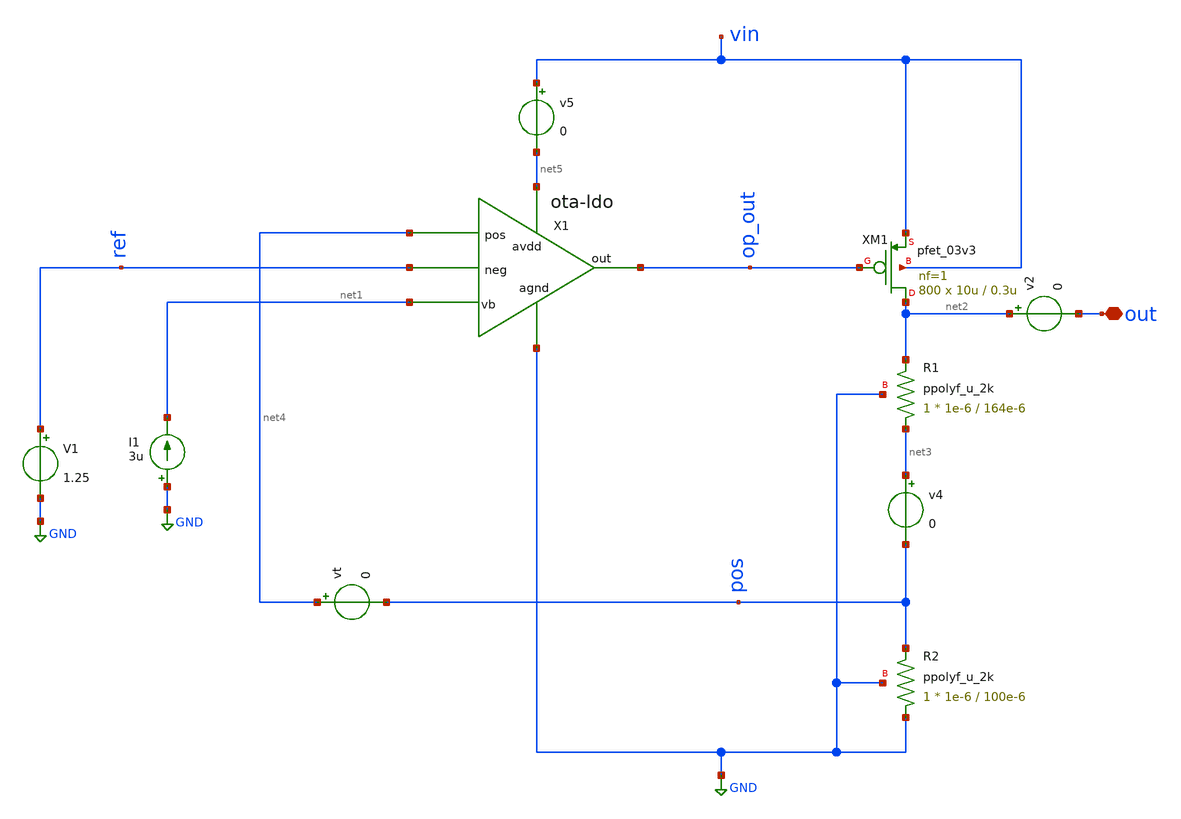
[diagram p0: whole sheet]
** sch_path: LDO/xschem/ldo/test/ldo-full-test.sch

.include $env(PDK_ROOT)/$env(PDK)/libs.tech/ngspice/design.ngspice
.lib $env(PDK_ROOT)/$env(PDK)/libs.tech/ngspice/sm141064.ngspice typical
.lib $env(PDK_ROOT)/$env(PDK)/libs.tech/ngspice/sm141064.ngspice mimcap_statistical
.lib $env(PDK_ROOT)/$env(PDK)/libs.tech/ngspice/sm141064.ngspice cap_mim
.lib $env(PDK_ROOT)/$env(PDK)/libs.tech/ngspice/sm141064.ngspice res_typical

**.subckt ldo-full-test out
*.iopin out
I1 GND net1 3u
V1 ref GND 1.25
XM1 net2 op_out vin vin pfet_03v3 L=0.3u W=10u nf=1 ad='int((nf+1)/2) * W/nf * 0.18u' as='int((nf+2)/2) * W/nf * 0.18u'
+ pd='2*int((nf+1)/2) * (W/nf + 0.18u)' ps='2*int((nf+2)/2) * (W/nf + 0.18u)' nrd='0.18u / W' nrs='0.18u / W'
+ sa=0 sb=0 sd=0 m=800
XR1 net3 net2 GND ppolyf_u_2k r_width=1e-6 r_length=164e-6 m=1
XR2 GND pos GND ppolyf_u_2k r_width=1e-6 r_length=100e-6 m=1
v4 net3 pos 0
X1 net5 op_out ref net4 net1 GND ota-ldo
vt net4 pos 0
v2 net2 out 0
v5 vin net5 0
**** begin user architecture code

.param R=66k
R10 out 0 {R}
IL out 0 PWL(0 0.1m 10u 0.1m 20u 10m 30u 10m)
*CL out 0 10p

Vs vin 0 PULSE(5 5 50u 20u 1u 100u 100u)

.nodeset v(out)=0
.nodeset v(x1.pos)=0

*TRANSIENT
.control
save all
tran 1ns 200us
let gds = @x1.xm2.m0[gds]
print ic
plot gds
plot v(out) v(ref) v(pos) v(vin)
plot i(v5)
*plot v(op_out)
*plot v(out)
*plot i(out)
*plot i(v3)*v(vin)
.endc



*SUPPLY SWEEP
.control
dc Vs 4 0 -0.01
plot v(out) v(ref) v(vin)
*plot v(x1.op_out)
*plot i(v.x1.v4)
.endc

*Stability_Analysis (openloop)
.control
alter Vs AC=0
alter Vt AC =1
ac dec 100 1 1G
plot vdb(out)
let phase_val = 180/PI*cph(out)
plot phase_val
meas ac pm FIND phase_val WHEN vdb(out)=0
*plot (180/pi)*vp(out)
*let gm0=@m.xm0.m0[gm]
*let Zout=(1.5)/(gm0*v(op_out))
*let Zout2=v(out)/gm0
*plot vdb(Zout2)
*wrdata /foss/designs/LDO_Design/data/data_PSRR.dat vdb(out)
.endc

*PSRR_Analysis
.control
alter Vs AC =1
alter Vt AC=0
ac dec 100 1 1G
plot vdb(out)
let phase_val = 180/PI*cph(out)
plot phase_val
*plot (180/pi)*vp(out)
*let gm0=@m.xm0.m0[gm]
*let Zout=(1.5)/(gm0*v(op_out))
*let Zout2=v(out)/gm0
*plot vdb(Zout2)
*wrdata /foss/designs/LDO_Design/data/data_PSRR.dat vdb(out)
.endc


**Load_Transient
.control
alter IL 50u
alter R10 3600k
tran 0.1u 100u
meas TRAN V_ldo_100u FIND v(out) AT=5u
meas TRAN V_ldo_10m FIND v(out) AT=100u
let load_reg= V_ldo_100u-V_ldo_10m
let load_current =(-1*i(Vs)-131.8e-6)
print load_reg
plot i(v2) v(out)-3.3
.endc



.control
alter R10 36k
alter @IL[pwl]=[ 0 0 10u 0 20u 0 30u 0 ]
alter @Vs[pulse]=[4 3.3 50u 1u 1u 10u 100u]
alter IL 0
tran 0.1u 100u
plot v(vin) v(out)
.endc

**** end user architecture code
**.ends

* expanding   symbol:  symbol/ota-ldo.sym # of pins=6
** sym_path: LDO/xschem/ota-ldo/ota-ldo.sym
** sch_path: LDO/xschem/ota-ldo/ota-ldo.sch
.subckt ota-ldo avdd out neg pos vb agnd
*.iopin vb
*.iopin avdd
*.iopin agnd
*.ipin neg
*.ipin pos
*.opin out
XC2 net2 out cap_mim_1f5fF c_width=50e-6 c_length=20e-6 m=1
XM1 net1 neg net3 agnd nfet_03v3 L=0.3u W=10u nf=1 ad='int((nf+1)/2) * W/nf * 0.18u' as='int((nf+2)/2) * W/nf * 0.18u'
+ pd='2*int((nf+1)/2) * (W/nf + 0.18u)' ps='2*int((nf+2)/2) * (W/nf + 0.18u)' nrd='0.18u / W' nrs='0.18u / W'
+ sa=0 sb=0 sd=0 m=1
XM3 net1 net1 avdd avdd pfet_03v3 L=0.8u W=9u nf=1 ad='int((nf+1)/2) * W/nf * 0.18u' as='int((nf+2)/2) * W/nf * 0.18u'
+ pd='2*int((nf+1)/2) * (W/nf + 0.18u)' ps='2*int((nf+2)/2) * (W/nf + 0.18u)' nrd='0.18u / W' nrs='0.18u / W'
+ sa=0 sb=0 sd=0 m=1
XM2 net2 pos net3 agnd nfet_03v3 L=0.3u W=10u nf=1 ad='int((nf+1)/2) * W/nf * 0.18u' as='int((nf+2)/2) * W/nf * 0.18u'
+ pd='2*int((nf+1)/2) * (W/nf + 0.18u)' ps='2*int((nf+2)/2) * (W/nf + 0.18u)' nrd='0.18u / W' nrs='0.18u / W'
+ sa=0 sb=0 sd=0 m=1
XM4 net2 net1 avdd avdd pfet_03v3 L=0.8u W=9u nf=1 ad='int((nf+1)/2) * W/nf * 0.18u' as='int((nf+2)/2) * W/nf * 0.18u'
+ pd='2*int((nf+1)/2) * (W/nf + 0.18u)' ps='2*int((nf+2)/2) * (W/nf + 0.18u)' nrd='0.18u / W' nrs='0.18u / W'
+ sa=0 sb=0 sd=0 m=1
XM7 net3 vb agnd agnd nfet_03v3 L=0.8u W=16u nf=1 ad='int((nf+1)/2) * W/nf * 0.18u' as='int((nf+2)/2) * W/nf * 0.18u'
+ pd='2*int((nf+1)/2) * (W/nf + 0.18u)' ps='2*int((nf+2)/2) * (W/nf + 0.18u)' nrd='0.18u / W' nrs='0.18u / W'
+ sa=0 sb=0 sd=0 m=1
XM8 vb vb agnd agnd nfet_03v3 L=0.8u W=1.66u nf=1 ad='int((nf+1)/2) * W/nf * 0.18u' as='int((nf+2)/2) * W/nf * 0.18u'
+ pd='2*int((nf+1)/2) * (W/nf + 0.18u)' ps='2*int((nf+2)/2) * (W/nf + 0.18u)' nrd='0.18u / W' nrs='0.18u / W'
+ sa=0 sb=0 sd=0 m=1
XM5 out net2 avdd avdd pfet_03v3 L=0.4u W=60u nf=1 ad='int((nf+1)/2) * W/nf * 0.18u' as='int((nf+2)/2) * W/nf * 0.18u'
+ pd='2*int((nf+1)/2) * (W/nf + 0.18u)' ps='2*int((nf+2)/2) * (W/nf + 0.18u)' nrd='0.18u / W' nrs='0.18u / W'
+ sa=0 sb=0 sd=0 m=1
XM6 out vb agnd agnd nfet_03v3 L=0.8u W=60u nf=1 ad='int((nf+1)/2) * W/nf * 0.18u' as='int((nf+2)/2) * W/nf * 0.18u'
+ pd='2*int((nf+1)/2) * (W/nf + 0.18u)' ps='2*int((nf+2)/2) * (W/nf + 0.18u)' nrd='0.18u / W' nrs='0.18u / W'
+ sa=0 sb=0 sd=0 m=1
.ends

.GLOBAL GND
.end
